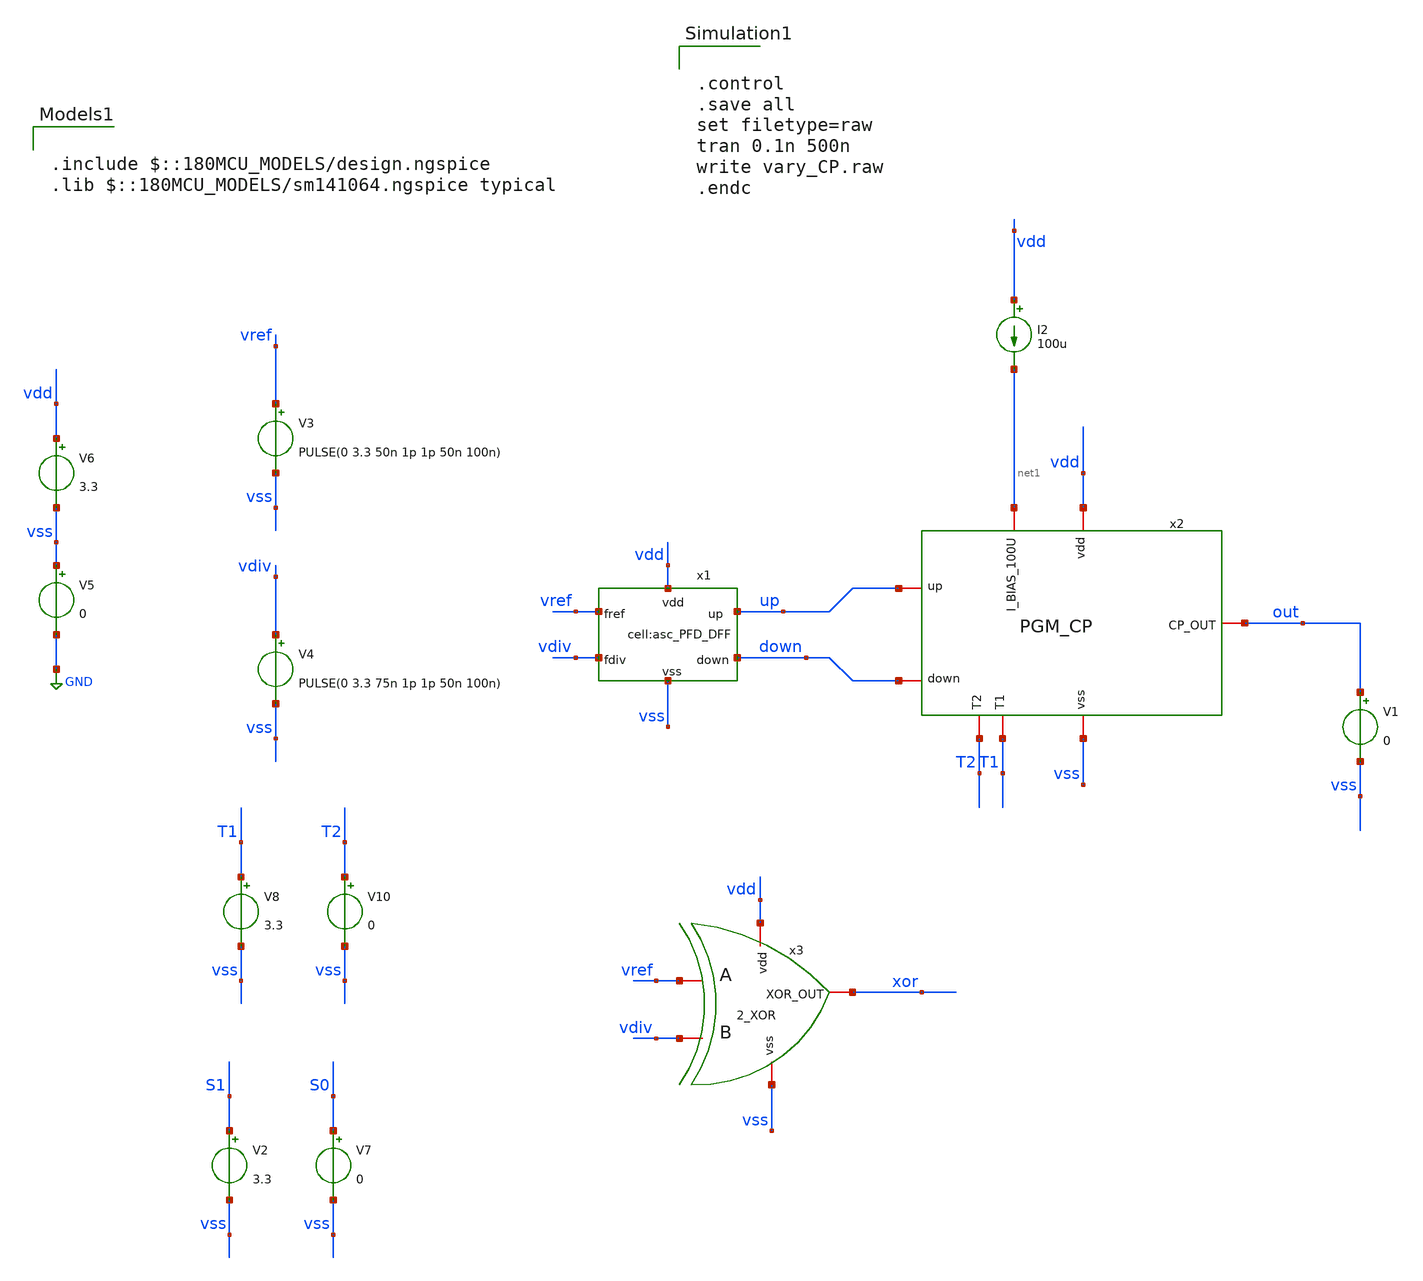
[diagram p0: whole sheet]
** sch_path: designs/libs/xp_tb_analog/tb_PFD_CP.sch
**.subckt tb_PFD_CP
V3 vref vss PULSE(0 3.3 50n 1p 1p 50n 100n)
V4 vdiv vss PULSE(0 3.3 75n 1p 1p 50n 100n)
x1 vdd vss down up vref vdiv asc_PFD_DFF
V5 vss GND 0
V6 vdd vss 3.3
V8 T1 vss 3.3
V10 T2 vss 0
x2 vdd out vss T1 T2 up down net1 PGM_CP
I2 vdd net1 100u
V1 out vss 0
V2 S1 vss 3.3
V7 S0 vss 0
x3 vref vdiv vss vdd xor 2_XOR
**** begin user architecture code

.include $::180MCU_MODELS/design.ngspice
.lib $::180MCU_MODELS/sm141064.ngspice typical



.control
.save all
set filetype=raw
tran 0.1n 500n
write vary_CP.raw
.endc


**** end user architecture code
**.ends
.GLOBAL GND
.end
